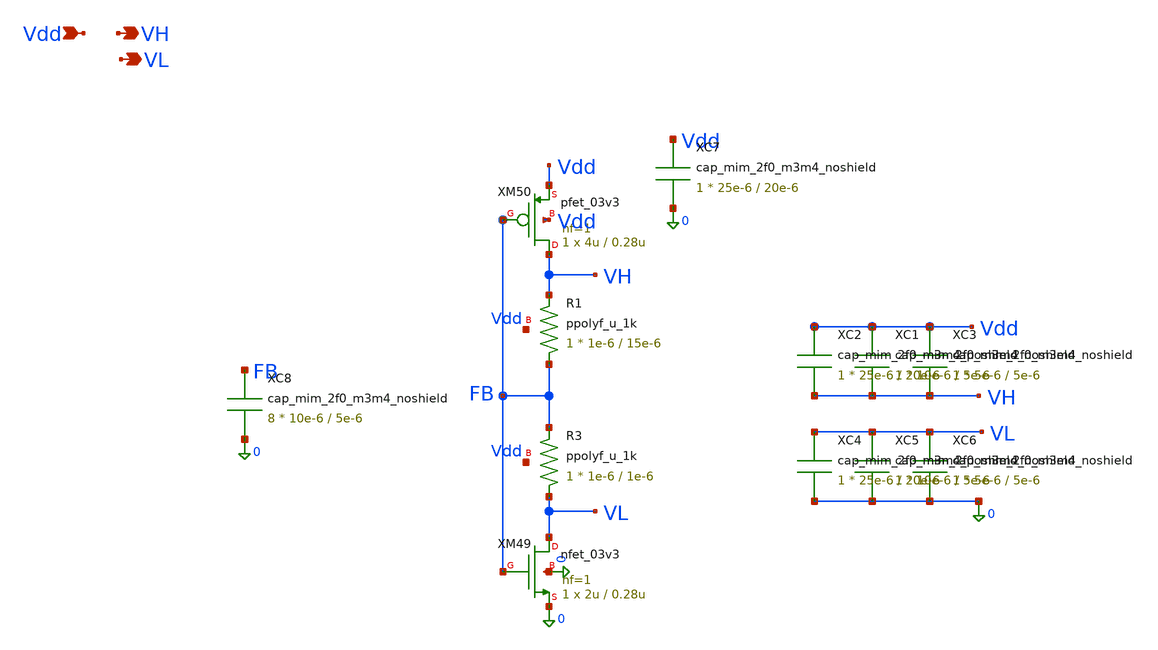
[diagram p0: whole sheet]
** sch_path: blocks/dac/cellv9/clamp.sch
**.subckt clamp VH VL Vdd
*.opin VH
*.opin VL
*.ipin Vdd
XM49 VL FB 0 0 nfet_03v3 L=0.28u W=2u nf=1 ad='int((nf+1)/2) * W/nf * 0.18u' as='int((nf+2)/2) * W/nf * 0.18u'
+ pd='2*int((nf+1)/2) * (W/nf + 0.18u)' ps='2*int((nf+2)/2) * (W/nf + 0.18u)' nrd='0.18u / W' nrs='0.18u / W'
+ sa=0 sb=0 sd=0 m=1
XM50 VH FB Vdd Vdd pfet_03v3 L=0.28u W=4u nf=1 ad='int((nf+1)/2) * W/nf * 0.18u' as='int((nf+2)/2) * W/nf * 0.18u'
+ pd='2*int((nf+1)/2) * (W/nf + 0.18u)' ps='2*int((nf+2)/2) * (W/nf + 0.18u)' nrd='0.18u / W' nrs='0.18u / W'
+ sa=0 sb=0 sd=0 m=1
XR3 VL FB Vdd ppolyf_u_1k r_width=1e-6 r_length=1e-6 m=1
XR1 FB VH Vdd ppolyf_u_1k r_width=1e-6 r_length=15e-6 m=1
XC2 Vdd VH cap_mim_2f0_m3m4_noshield c_width=25e-6 c_length=20e-6 m=1
XC1 Vdd VH cap_mim_2f0_m3m4_noshield c_width=10e-6 c_length=5e-6 m=1
XC3 Vdd VH cap_mim_2f0_m3m4_noshield c_width=5e-6 c_length=5e-6 m=1
XC4 VL 0 cap_mim_2f0_m3m4_noshield c_width=25e-6 c_length=20e-6 m=1
XC5 VL 0 cap_mim_2f0_m3m4_noshield c_width=10e-6 c_length=5e-6 m=1
XC6 VL 0 cap_mim_2f0_m3m4_noshield c_width=5e-6 c_length=5e-6 m=1
XC7 Vdd 0 cap_mim_2f0_m3m4_noshield c_width=25e-6 c_length=20e-6 m=1
XC8 FB 0 cap_mim_2f0_m3m4_noshield c_width=10e-6 c_length=5e-6 m=8
**.ends
.end
